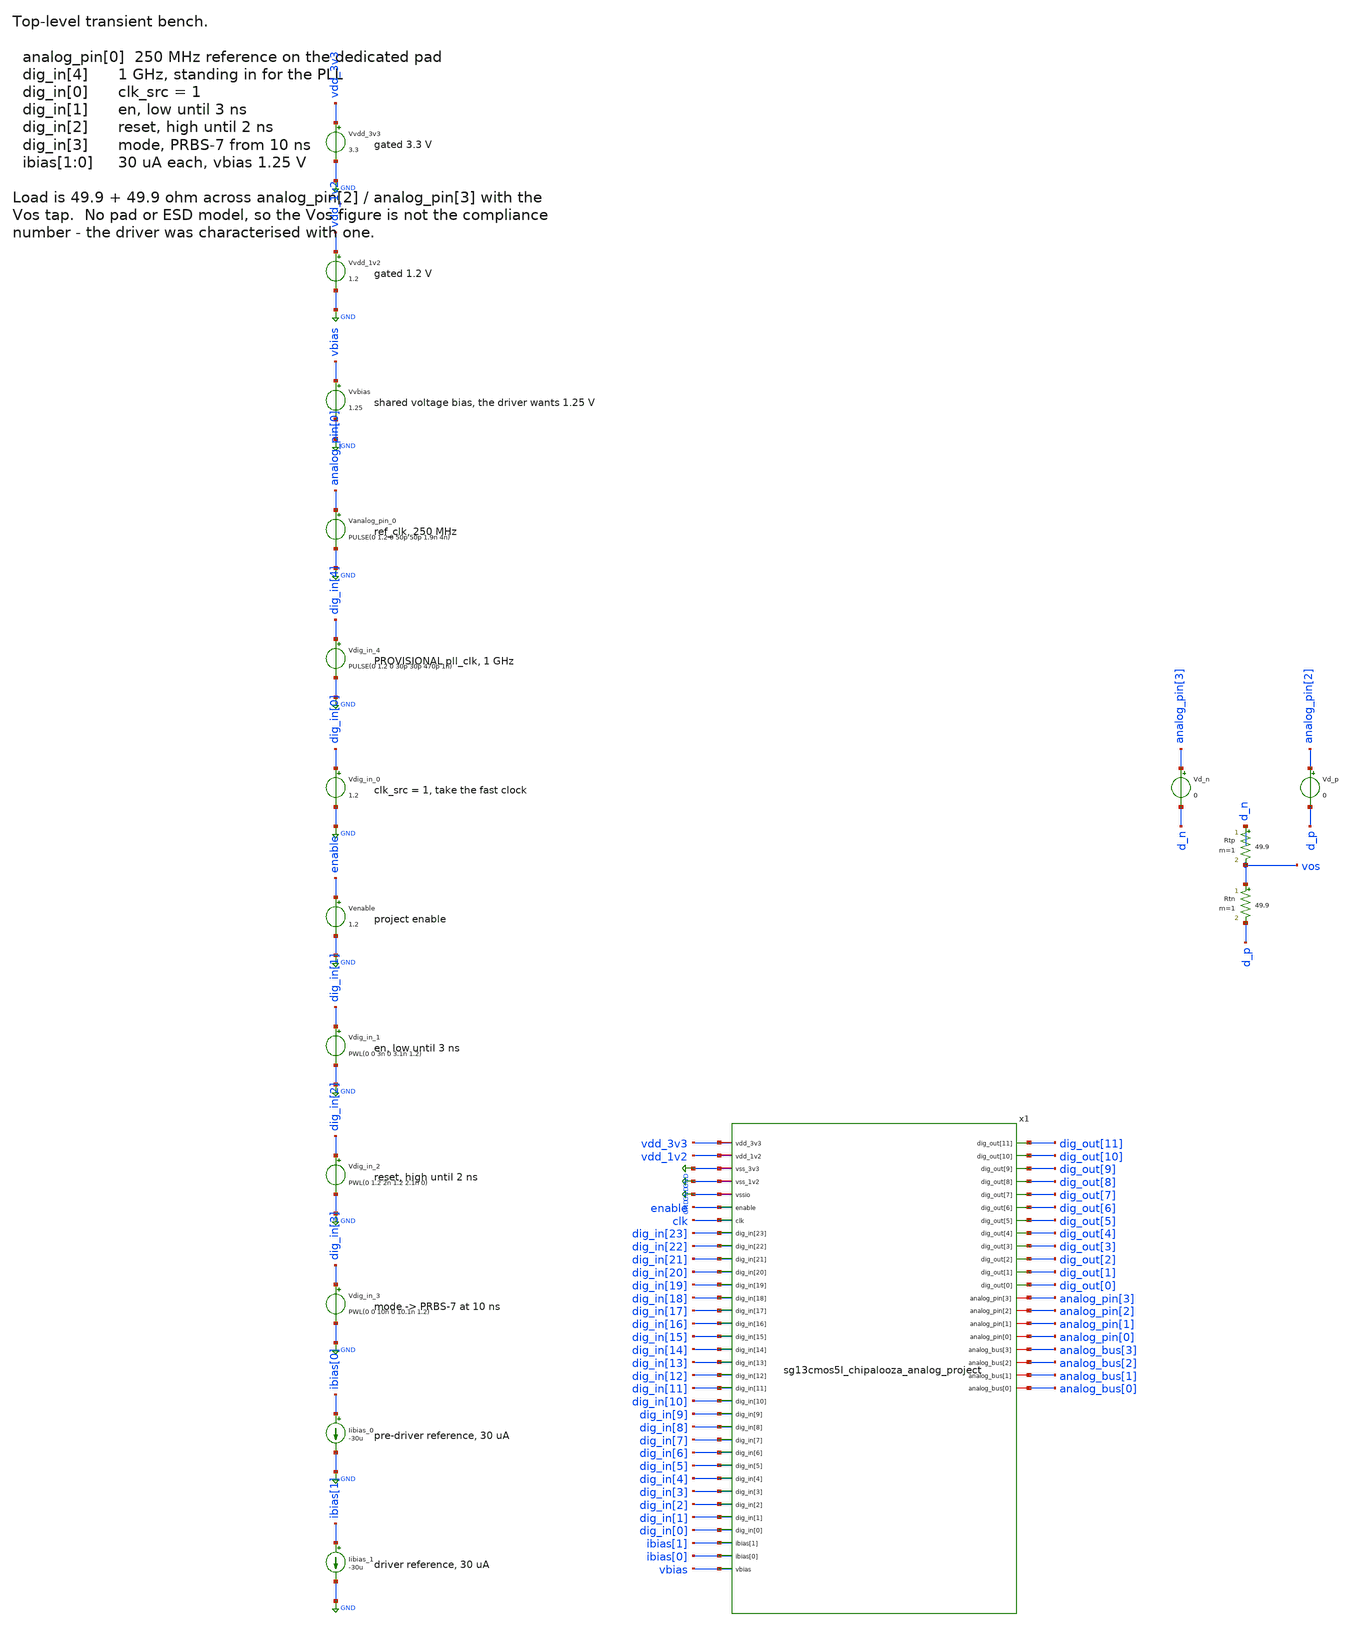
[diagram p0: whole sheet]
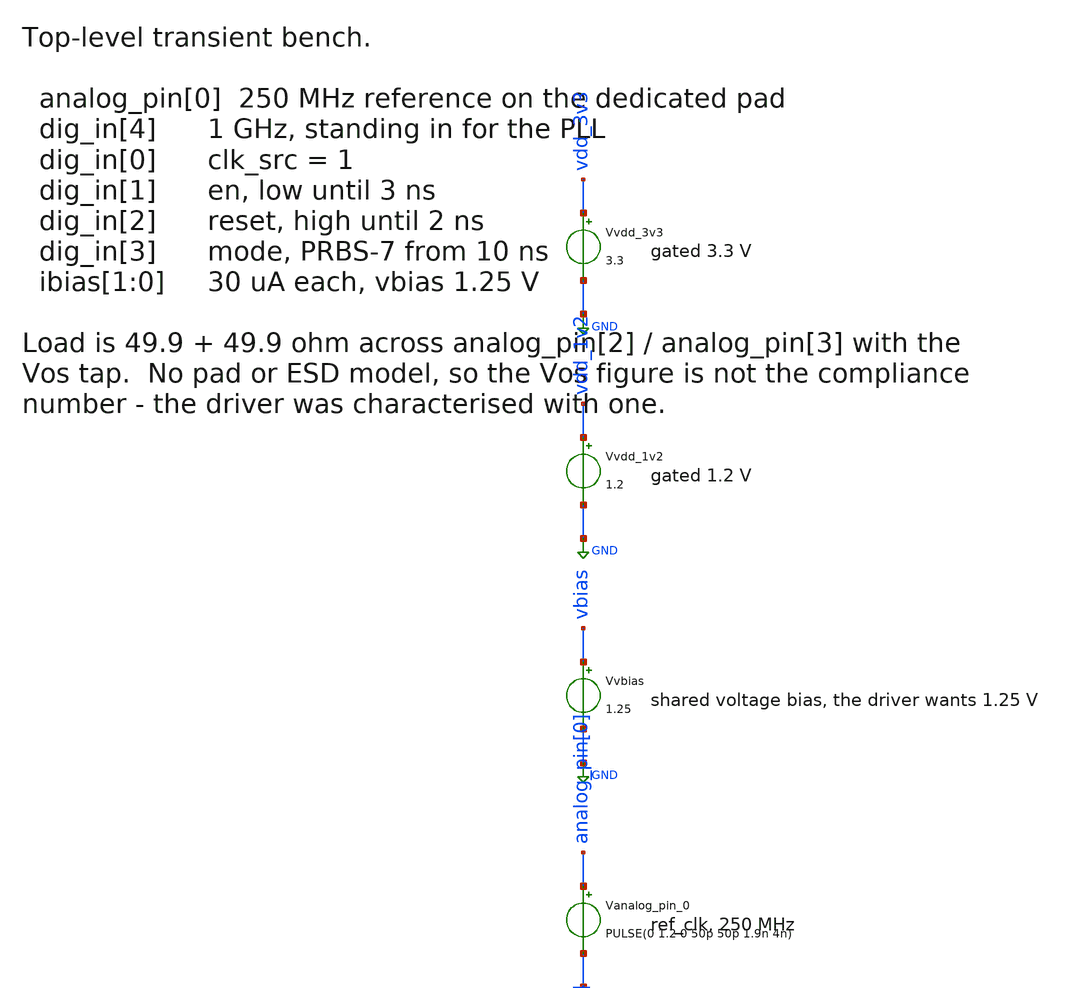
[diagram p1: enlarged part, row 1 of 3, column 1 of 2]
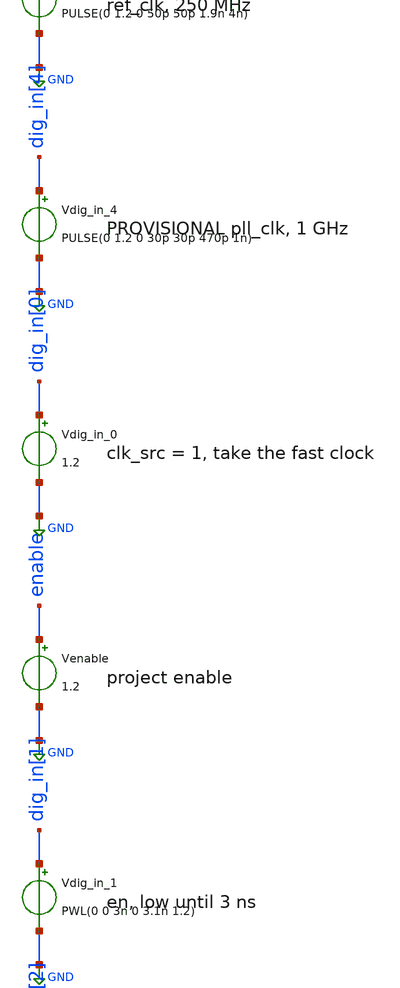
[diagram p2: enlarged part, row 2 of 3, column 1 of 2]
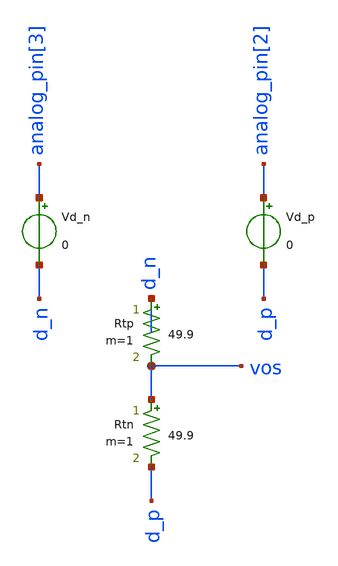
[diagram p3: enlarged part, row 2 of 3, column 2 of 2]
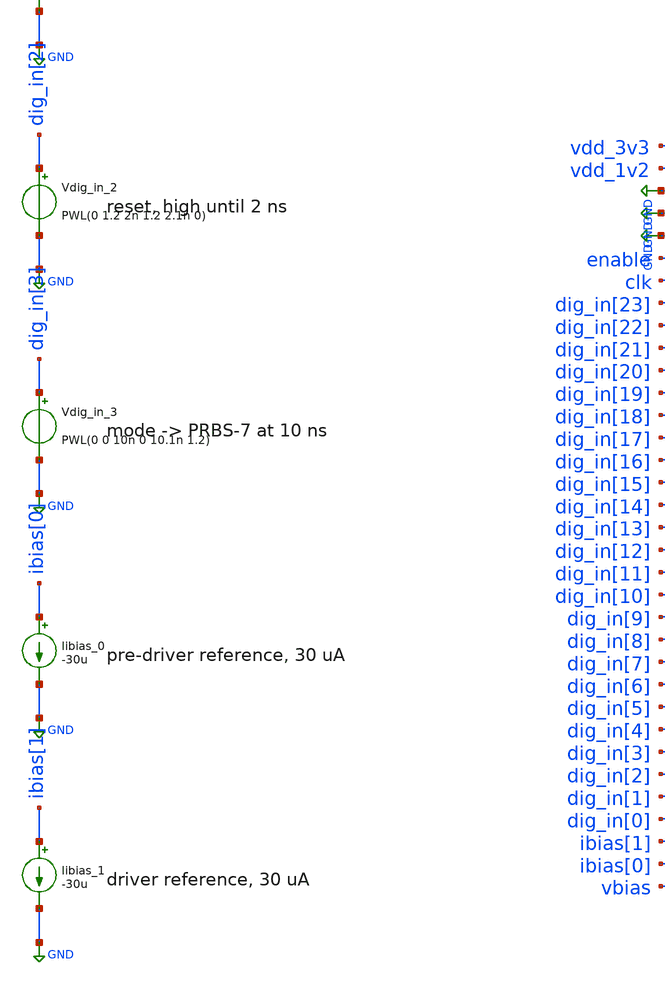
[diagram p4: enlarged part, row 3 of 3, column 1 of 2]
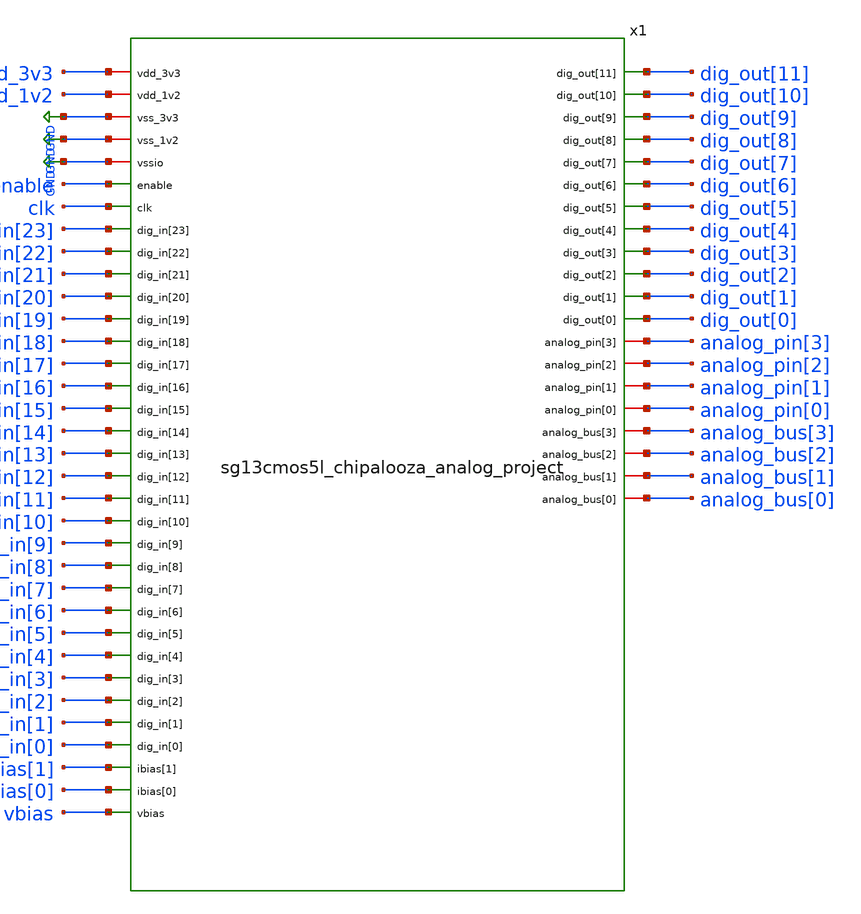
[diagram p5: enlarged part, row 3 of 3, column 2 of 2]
** sch_path: testbenches/xschem/sg13cmos5l_chipalooza_analog_project_tb_tran.sch
**.subckt sg13cmos5l_chipalooza_analog_project_tb_tran
Vvdd_3v3 vdd_3v3 GND 3.3
Vvdd_1v2 vdd_1v2 GND 1.2
Vvbias vbias GND 1.25
Vanalog_pin_0 analog_pin[0] GND PULSE(0 1.2 0 50p 50p 1.9n 4n)
Vdig_in_4 dig_in[4] GND PULSE(0 1.2 0 30p 30p 470p 1n)
Vdig_in_0 dig_in[0] GND 1.2
Venable enable GND 1.2
Vdig_in_1 dig_in[1] GND PWL(0 0 3n 0 3.1n 1.2)
Vdig_in_2 dig_in[2] GND PWL(0 1.2 2n 1.2 2.1n 0)
Vdig_in_3 dig_in[3] GND PWL(0 0 10n 0 10.1n 1.2)
Iibias_0 ibias[0] GND -30u
Iibias_1 ibias[1] GND -30u
x1 vdd_3v3 vdd_1v2 GND GND GND enable clk dig_in[23] dig_in[22] dig_in[21] dig_in[20] dig_in[19]
+ dig_in[18] dig_in[17] dig_in[16] dig_in[15] dig_in[14] dig_in[13] dig_in[12] dig_in[11] dig_in[10] dig_in[9]
+ dig_in[8] dig_in[7] dig_in[6] dig_in[5] dig_in[4] dig_in[3] dig_in[2] dig_in[1] dig_in[0] ibias[1] ibias[0]
+ vbias dig_out[11] dig_out[10] dig_out[9] dig_out[8] dig_out[7] dig_out[6] dig_out[5] dig_out[4]
+ dig_out[3] dig_out[2] dig_out[1] dig_out[0] analog_pin[3] analog_pin[2] analog_pin[1] analog_pin[0]
+ analog_bus[3] analog_bus[2] analog_bus[1] analog_bus[0] sg13cmos5l_chipalooza_analog_project
Vd_n analog_pin[3] d_n 0
Vd_p analog_pin[2] d_p 0
Rtp d_n vos 49.9 m=1
Rtn vos d_p 49.9 m=1
**** begin user architecture code


.lib cornerMOSlv.lib mos_tt
.lib cornerMOShv.lib mos_tt
.lib cornerRES.lib res_typ
.lib cornerDIO.lib dio_tt
.include cap_mfringe.lib
.include /foss/pdks/ihp-sg13cmos5l/libs.ref/sg13cmos5l_stdcell/spice/sg13cmos5l_stdcell.spice
.temp 27
.options savecurrents klu method=gear reltol=1e-3 abstol=1e-12 gmin=1e-12
.control
save all
op
remzerovec
write @schname\.raw
set appendwrite
tran 5p 40n
write @schname\.raw

let vod = v(d_p)-v(d_n)
meas tran vod_max MAX vod from=20n to=40n
meas tran vod_min MIN vod from=20n to=40n
meas tran vos_avg AVG v(vos) from=20n to=40n
meas tran vos_max MAX v(vos) from=20n to=40n
meas tran vos_min MIN v(vos) from=20n to=40n
let vos_pp = vos_max - vos_min
print vod_max vod_min vos_avg vos_pp

unset appendwrite
set wr_vecnames
set wr_singlescale
wrdata ../plot_simulations/data/@schname\.txt  v(d_p) v(d_n) v(vos) vod v(x1.core_p) v(x1.core_n)
.endc


**** end user architecture code
**.ends

* expanding   symbol:  sg13cmos5l_chipalooza_analog_project.sym # of pins=54
** sym_path: schematic/xschem/sg13cmos5l_chipalooza_analog_project.sym
** sch_path: schematic/xschem/sg13cmos5l_chipalooza_analog_project.sch
.subckt sg13cmos5l_chipalooza_analog_project vdd_3v3 vdd_1v2 vss_3v3 vss_1v2 vssio enable clk
+ dig_in[23] dig_in[22] dig_in[21] dig_in[20] dig_in[19] dig_in[18] dig_in[17] dig_in[16] dig_in[15] dig_in[14]
+ dig_in[13] dig_in[12] dig_in[11] dig_in[10] dig_in[9] dig_in[8] dig_in[7] dig_in[6] dig_in[5] dig_in[4]
+ dig_in[3] dig_in[2] dig_in[1] dig_in[0] ibias[1] ibias[0] vbias dig_out[11] dig_out[10] dig_out[9] dig_out[8]
+ dig_out[7] dig_out[6] dig_out[5] dig_out[4] dig_out[3] dig_out[2] dig_out[1] dig_out[0] analog_pin[3]
+ analog_pin[2] analog_pin[1] analog_pin[0] analog_bus[3] analog_bus[2] analog_bus[1] analog_bus[0]
*.iopin vdd_3v3
*.iopin vdd_1v2
*.iopin vss_3v3
*.iopin vss_1v2
*.iopin vssio
*.ipin enable
*.ipin clk
*.ipin dig_in[23]
*.ipin dig_in[22]
*.ipin dig_in[21]
*.ipin dig_in[20]
*.ipin dig_in[19]
*.ipin dig_in[18]
*.ipin dig_in[17]
*.ipin dig_in[16]
*.ipin dig_in[15]
*.ipin dig_in[14]
*.ipin dig_in[13]
*.ipin dig_in[12]
*.ipin dig_in[11]
*.ipin dig_in[10]
*.ipin dig_in[9]
*.ipin dig_in[8]
*.ipin dig_in[7]
*.ipin dig_in[6]
*.ipin dig_in[5]
*.ipin dig_in[4]
*.ipin dig_in[3]
*.ipin dig_in[2]
*.ipin dig_in[1]
*.ipin dig_in[0]
*.opin dig_out[11]
*.opin dig_out[10]
*.opin dig_out[9]
*.opin dig_out[8]
*.opin dig_out[7]
*.opin dig_out[6]
*.opin dig_out[5]
*.opin dig_out[4]
*.opin dig_out[3]
*.opin dig_out[2]
*.opin dig_out[1]
*.opin dig_out[0]
*.iopin analog_pin[3]
*.iopin analog_pin[2]
*.iopin analog_pin[1]
*.iopin analog_pin[0]
*.ipin ibias[1]
*.ipin ibias[0]
*.ipin vbias
*.iopin analog_bus[3]
*.iopin analog_bus[2]
*.iopin analog_bus[1]
*.iopin analog_bus[0]
xpat analog_pin[0] dig_in[4] dig_in[0] en_gated dig_in[2] dig_in[3] core_p core_n vdd_1v2 vss_1v2
+ lvds_pattern
xlvds core_p core_n ibias[0] ibias[1] vbias vdd_3v3 analog_pin[2] analog_pin[3] vss_3v3 lvds_tx
xeng en_gated enable dig_in[1] vdd_1v2 vss_1v2 sg13cmos5l_and2_1
XCd12 vss_1v2 vdd_1v2 vss_1v2 vss_1v2 sg13_lv_pmos w=10.0u l=10.0u ng=1 m=1 mm_ok=1
XCd33 vss_3v3 vdd_3v3 vss_3v3 vss_3v3 sg13_hv_pmos w=10.0u l=10.0u ng=1 m=1 mm_ok=1
.ends


* expanding   symbol:  lvds_pattern.sym # of pins=10
** sym_path: macros/lvds_pattern/schematic/xschem/lvds_pattern.sym
** sch_path: macros/lvds_pattern/schematic/xschem/lvds_pattern.sch
.subckt lvds_pattern ref_clk pll_clk clk_src en reset mode D_p D_n VDD VSS
*.ipin ref_clk
*.ipin pll_clk
*.ipin clk_src
*.ipin en
*.ipin reset
*.ipin mode
*.opin D_p
*.opin D_n
*.iopin VDD
*.iopin VSS
xcsel clk_sel ref_clk pll_clk clk_src VDD VSS sg13cmos5l_mux2_2
xicg gclk clk_sel en VDD VSS sg13cmos5l_lgcp_1
xclkb gclk_b gclk VDD VSS sg13cmos5l_buf_4
xicg2 gclk_free clk_sel VDD VDD VSS sg13cmos5l_lgcp_1
xclkb2 gclk_free_b gclk_free VDD VSS sg13cmos5l_buf_4
xrstb reset_b reset VDD VSS sg13cmos5l_inv_2
xs0 s0 s0_n gclk_b fb reset_b VDD VSS sg13cmos5l_dfrbp_2
xs1 s1 s1_n gclk_b s0 reset_b VDD VSS sg13cmos5l_dfrbp_2
xs2 s2 s2_n gclk_b s1 reset_b VDD VSS sg13cmos5l_dfrbp_2
xs3 s3 s3_n gclk_b s2 reset_b VDD VSS sg13cmos5l_dfrbp_2
xs4 s4 s4_n gclk_b s3 reset_b VDD VSS sg13cmos5l_dfrbp_2
xs5 s5 s5_n gclk_b s4 reset_b VDD VSS sg13cmos5l_dfrbp_2
xs6 s6 s6_n gclk_b s5 reset_b VDD VSS sg13cmos5l_dfrbp_2
xfb fb s6 s5 VDD VSS sg13cmos5l_xnor2_1
xclkn gclk_bn gclk_b VDD VSS sg13cmos5l_inv_2
xmodep dp0 gclk_bn fp mode VDD VSS sg13cmos5l_mux2_2
xmoden dn0 gclk_b fn mode VDD VSS sg13cmos5l_mux2_2
xp1 dp1 dp0 VDD VSS sg13cmos5l_inv_2
xp2 dp2 dp1 VDD VSS sg13cmos5l_inv_8
xbp D_p dp2 VDD VSS sg13cmos5l_inv_16
xn1 dn1 dn0 VDD VSS sg13cmos5l_inv_2
xn2 dn2 dn1 VDD VSS sg13cmos5l_inv_8
xbn D_n dn2 VDD VSS sg13cmos5l_inv_16
xffn fn fn_n gclk_free_b s6_n VDD VSS VSS reset_b VDD VSS sg13cmos5l_sdfbbp_1
xffp fp fp_n gclk_free_b s6 reset_b VSS VSS VDD VDD VSS sg13cmos5l_sdfbbp_1
x1 VDD VSS sg13cmos5l_decap_4
x2 VDD VSS sg13cmos5l_decap_4
x3 VDD VSS sg13cmos5l_decap_4
x4 VDD VSS sg13cmos5l_decap_4
x5 VDD VSS sg13cmos5l_decap_4
x6 VDD VSS sg13cmos5l_decap_4
x7 VDD VSS sg13cmos5l_decap_8
x8 VDD VSS sg13cmos5l_decap_8
x9 VDD VSS sg13cmos5l_decap_8
x10 VDD VSS sg13cmos5l_decap_8
x11 VDD VSS sg13cmos5l_decap_8
x12 VDD VSS sg13cmos5l_decap_8
x13 VDD VSS sg13cmos5l_decap_8
x14 VDD VSS sg13cmos5l_decap_8
x15 VDD VSS sg13cmos5l_decap_8
x16 VDD VSS sg13cmos5l_decap_8
x17 VDD VSS sg13cmos5l_decap_8
x18 VDD VSS sg13cmos5l_decap_8
x19 VDD VSS sg13cmos5l_decap_8
x20 VDD VSS sg13cmos5l_decap_8
x21 VDD VSS sg13cmos5l_decap_8
x22 VDD VSS sg13cmos5l_decap_8
x23 VDD VSS sg13cmos5l_decap_8
x24 VDD VSS sg13cmos5l_decap_8
x25 VDD VSS sg13cmos5l_decap_8
x26 VDD VSS sg13cmos5l_decap_8
x27 VDD VSS sg13cmos5l_decap_8
x28 VDD VSS sg13cmos5l_decap_8
x29 VDD VSS sg13cmos5l_decap_8
x30 VDD VSS sg13cmos5l_decap_8
x31 VDD VSS sg13cmos5l_decap_8
x32 VDD VSS sg13cmos5l_decap_8
x33 VDD VSS sg13cmos5l_decap_8
x34 VDD VSS sg13cmos5l_decap_8
x35 VDD VSS sg13cmos5l_decap_8
x36 VDD VSS sg13cmos5l_decap_8
x37 VDD VSS sg13cmos5l_decap_8
x38 VDD VSS sg13cmos5l_decap_8
x39 VDD VSS sg13cmos5l_decap_8
x40 VDD VSS sg13cmos5l_decap_8
x41 VDD VSS sg13cmos5l_decap_8
.ends


* expanding   symbol:  lvds_tx.sym # of pins=9
** sym_path: macros/lvds_tx/schematic/xschem/lvds_tx.sym
** sch_path: macros/lvds_tx/schematic/xschem/lvds_tx.sch
.subckt lvds_tx D_p D_n Iref_pd Iref_drv Vref Va Out_p Out_n Vss
*.ipin D_p
*.ipin D_n
*.ipin Iref_pd
*.ipin Iref_drv
*.ipin Vref
*.iopin Va
*.iopin Vss
*.opin Out_p
*.opin Out_n
Xpd D_p D_n Iref_pd In_p In_n Va Vss predriver
Xdrv Va Out_p In_p In_n Iref_drv Vref Out_n Vss Driver
.ends


* expanding   symbol:  predriver.sym # of pins=7
** sym_path: macros/lvds_tx/schematic/xschem/predriver.sym
** sch_path: macros/lvds_tx/schematic/xschem/predriver.sch
.subckt predriver D_p D_n Iref In_p In_n Va Vss
*.iopin Va
*.iopin Vss
*.ipin Iref
*.ipin D_p
*.ipin D_n
*.opin In_p
*.opin In_n
Xkpm D_p D_n Iref net1 Va Vss predriver_comp
XMref Iref Iref Vss Vss sg13_hv_nmos w=2u l=2u ng=1 m=1 mm_ok=1
Xknm D_n D_p Iref net2 Va Vss predriver_comp
Xstm net1 net2 In_p In_n Va Vss predriver_stage
.ends


* expanding   symbol:  Driver.sym # of pins=8
** sym_path: macros/lvds_tx/schematic/xschem/Driver.sym
** sch_path: macros/lvds_tx/schematic/xschem/Driver.sch
.subckt Driver Va Out_p In_p In_n Iref Vref Out_n Vss
*.iopin Va
*.iopin Vss
*.opin Out_p
*.opin Out_n
*.ipin In_p
*.ipin In_n
*.ipin Iref
*.ipin Vref
XCtn1 Va tail_n Va Va sg13_hv_pmos w=11.8u l=5.25u ng=2 m=1 mm_ok=1
XCtn2 Va tail_n Va Va sg13_hv_pmos w=5.7u l=5.8u ng=2 m=1 mm_ok=1
XM2 tail_p cmfb Va Va sg13_hv_pmos w=97.2u l=0.5u ng=20 m=1 mm_ok=1
XM5 Out_p In_p tail_p Va sg13_hv_pmos w=80u l=0.4u ng=16 m=1 mm_ok=1
XM4 Out_n In_n tail_p Va sg13_hv_pmos w=80u l=0.4u ng=16 m=1 mm_ok=1
XM1 Out_p In_p tail_n Vss sg13_hv_nmos w=30u l=0.45u ng=15 m=1 mm_ok=1
XM3 Out_n In_n tail_n Vss sg13_hv_nmos w=30u l=0.45u ng=15 m=1 mm_ok=1
XM6 tail_n Iref Vss Vss sg13_hv_nmos w=49.6u l=0.5u ng=31 m=2 mm_ok=1
XM9 Iref Iref Vss Vss sg13_hv_nmos w=0.8u l=0.5u ng=1 m=1 mm_ok=1
XM13 pd pd Va Va sg13_hv_pmos w=5u l=1u ng=1 m=1 mm_ok=1
XM14 cmfb pd Va Va sg13_hv_pmos w=5u l=1u ng=1 m=1 mm_ok=1
XM11 pd cm otail Vss sg13_hv_nmos w=40u l=1u ng=16 m=1 mm_ok=1
XM12 cmfb Vref otail Vss sg13_hv_nmos w=40u l=1u ng=16 m=1 mm_ok=1
XM10 otail Iref Vss Vss sg13_hv_nmos w=0.8u l=0.5u ng=1 m=1 mm_ok=1
XCc Va cc_g Va Va sg13_hv_pmos w=50u l=5u ng=10 m=1 mm_ok=1
XRc cmfb cc_g Vss rppd w=1u l=6u m=1 b=0 mm_ok=1
XRp Out_p cm Vss rhigh w=1u l=7.35u m=1 b=0 mm_ok=1
XRn Out_n cm Vss rhigh w=1u l=7.35u m=1 b=0 mm_ok=1
XCxp Out_p In_n cap_cmomf w=5.913u l=5.913u mmin=1 mmax=4 subblock=0 rfmodel=0 subscale=1 m=1
+ mm_ok=1
XCxn Out_n In_p cap_cmomf w=5.913u l=5.913u mmin=1 mmax=4 subblock=0 rfmodel=0 subscale=1 m=1
+ mm_ok=1
XCop Vss Out_p Vss Vss sg13_hv_nmos w=10u l=5u ng=1 m=2 mm_ok=1
XCon Vss Out_n Vss Vss sg13_hv_nmos w=10u l=5u ng=1 m=2 mm_ok=1
.ends


* expanding   symbol:  predriver_comp.sym # of pins=6
** sym_path: macros/lvds_tx/schematic/xschem/predriver_comp.sym
** sch_path: macros/lvds_tx/schematic/xschem/predriver_comp.sch
.subckt predriver_comp Gin Din Iref Out Va Vss
*.iopin Va
*.iopin Vss
*.opin Out
*.ipin Din
*.ipin Gin
*.ipin Iref
XMld net1 net1 Va Va sg13_hv_pmos w=12u l=0.4u ng=4 m=1 mm_ok=1
XMlo Out net1 Va Va sg13_hv_pmos w=12u l=0.4u ng=4 m=1 mm_ok=1
XMid net1 Din net2 Vss sg13_hv_nmos w=24u l=0.45u ng=6 m=1 mm_ok=1
XMio Out Gin net2 Vss sg13_hv_nmos w=24u l=0.45u ng=6 m=1 mm_ok=1
XMt net2 Iref Vss Vss sg13_hv_nmos w=17.52u l=0.45u ng=6 m=2 mm_ok=1
.ends


* expanding   symbol:  predriver_stage.sym # of pins=6
** sym_path: macros/lvds_tx/schematic/xschem/predriver_stage.sym
** sch_path: macros/lvds_tx/schematic/xschem/predriver_stage.sch
.subckt predriver_stage In_p In_n Out_p Out_n Va Vss
*.ipin In_p
*.opin Out_p
*.ipin In_n
*.opin Out_n
*.iopin Va
*.iopin Vss
XMpp0 net1 In_p Va Va sg13_hv_pmos w=2.64u l=0.4u ng=1 m=1 mm_ok=1
XMnp0 net1 In_p Vss Vss sg13_hv_nmos w=1.6u l=0.45u ng=1 m=1 mm_ok=1
XMpp1 net2 net1 Va Va sg13_hv_pmos w=12.52u l=0.4u ng=4 m=1 mm_ok=1
XMnp1 net2 net1 Vss Vss sg13_hv_nmos w=5u l=0.45u ng=4 m=1 mm_ok=1
XMpp2 Out_p net2 Va Va sg13_hv_pmos w=40u l=0.4u ng=10 m=1 mm_ok=1
XMnp2 Out_p net2 Vss Vss sg13_hv_nmos w=16u l=0.45u ng=10 m=1 mm_ok=1
XMpn0 net3 In_n Va Va sg13_hv_pmos w=2.64u l=0.4u ng=1 m=1 mm_ok=1
XMnn0 net3 In_n Vss Vss sg13_hv_nmos w=1.6u l=0.45u ng=1 m=1 mm_ok=1
XMpn1 net4 net3 Va Va sg13_hv_pmos w=12.52u l=0.4u ng=4 m=1 mm_ok=1
XMnn1 net4 net3 Vss Vss sg13_hv_nmos w=5u l=0.45u ng=4 m=1 mm_ok=1
XMpn2 Out_n net4 Va Va sg13_hv_pmos w=40u l=0.4u ng=10 m=1 mm_ok=1
XMnn2 Out_n net4 Vss Vss sg13_hv_nmos w=16u l=0.45u ng=10 m=1 mm_ok=1
XMpxp net4 net2 Va Va sg13_hv_pmos w=4.38u l=0.4u ng=1 m=1 mm_ok=1
XMnxp net4 net2 Vss Vss sg13_hv_nmos w=1.75u l=0.45u ng=1 m=1 mm_ok=1
XMpxn net2 net4 Va Va sg13_hv_pmos w=4.38u l=0.4u ng=1 m=1 mm_ok=1
XMnxn net2 net4 Vss Vss sg13_hv_nmos w=1.75u l=0.45u ng=1 m=1 mm_ok=1
.ends

.GLOBAL GND
.end
